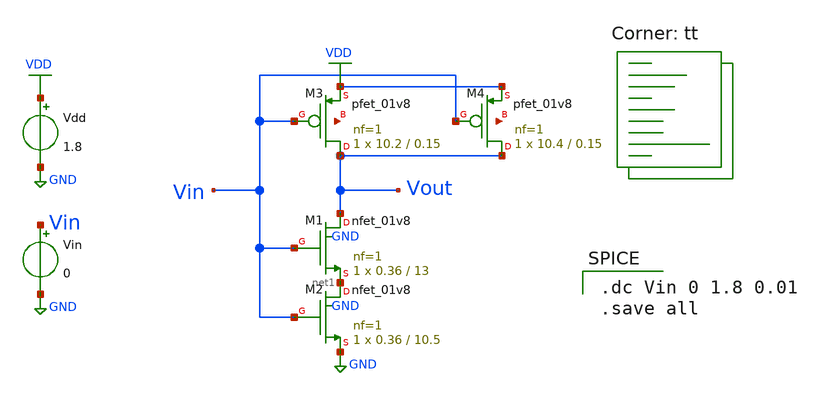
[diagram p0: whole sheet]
** sch_path: vdd1.8V/inverter_sat_13.sch
**.subckt inverter_sat_13
Vdd VDD GND 1.8
XM1 Vout Vin net1 GND sky130_fd_pr__nfet_01v8 L=13 W=0.36 nf=1 ad='int((nf+1)/2) * W/nf * 0.29' as='int((nf+2)/2) * W/nf * 0.29'
+ pd='2*int((nf+1)/2) * (W/nf + 0.29)' ps='2*int((nf+2)/2) * (W/nf + 0.29)' nrd='0.29 / W' nrs='0.29 / W'
+ sa=0 sb=0 sd=0 mult=1 m=1
Vin Vin GND 0
XM3 Vout Vin VDD net2 sky130_fd_pr__pfet_01v8 L=0.15 W=10.2 nf=1 ad='int((nf+1)/2) * W/nf * 0.29' as='int((nf+2)/2) * W/nf * 0.29'
+ pd='2*int((nf+1)/2) * (W/nf + 0.29)' ps='2*int((nf+2)/2) * (W/nf + 0.29)' nrd='0.29 / W' nrs='0.29 / W'
+ sa=0 sb=0 sd=0 mult=1 m=1
XM2 net1 Vin GND GND sky130_fd_pr__nfet_01v8 L=10.5 W=0.36 nf=1 ad='int((nf+1)/2) * W/nf * 0.29' as='int((nf+2)/2) * W/nf * 0.29'
+ pd='2*int((nf+1)/2) * (W/nf + 0.29)' ps='2*int((nf+2)/2) * (W/nf + 0.29)' nrd='0.29 / W' nrs='0.29 / W'
+ sa=0 sb=0 sd=0 mult=1 m=1
XM4 Vout Vin VDD net3 sky130_fd_pr__pfet_01v8 L=0.15 W=10.4 nf=1 ad='int((nf+1)/2) * W/nf * 0.29' as='int((nf+2)/2) * W/nf * 0.29'
+ pd='2*int((nf+1)/2) * (W/nf + 0.29)' ps='2*int((nf+2)/2) * (W/nf + 0.29)' nrd='0.29 / W' nrs='0.29 / W'
+ sa=0 sb=0 sd=0 mult=1 m=1
**** begin user architecture code

.dc Vin 0 1.8 0.01
.save all

.lib $::SKYWATER_MODELS/sky130.lib.spice tt
**** end user architecture code
**.ends
.GLOBAL GND
.GLOBAL VDD
.end
